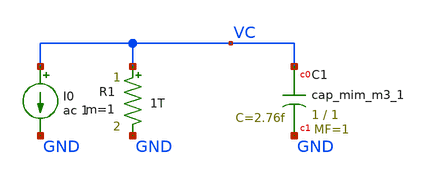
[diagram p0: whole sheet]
** sch_path: sim/unit_cap_mismatch.sch
.lib $::SKYWATER_MODELS/sky130.lib.spice tt_mm

**.subckt unit_cap_mismatch
XC1 VC GND sky130_fd_pr__cap_mim_m3_1 W=1 L=1 MF=1 m=1
I0 VC GND ac 1
R1 VC GND 1T m=1
**** begin user architecture code


.save all
.control
		echo > unit_cap_mismatch.txt
		if run > 0
      			reset
      			set appendwrite
    		end
		let run=0
  		dowhile run <= 200
		print run
		ac dec 10 10Meg 100Meg
		meas ac vcap find vm(vc) AT=100e6
		write unit_cap_mismatch.raw
		echo $&vcap >> unit_cap_mismatch.txt
    		let run = run + 1
		reset
  	end
.endc


**** end user architecture code
**.ends
.end
